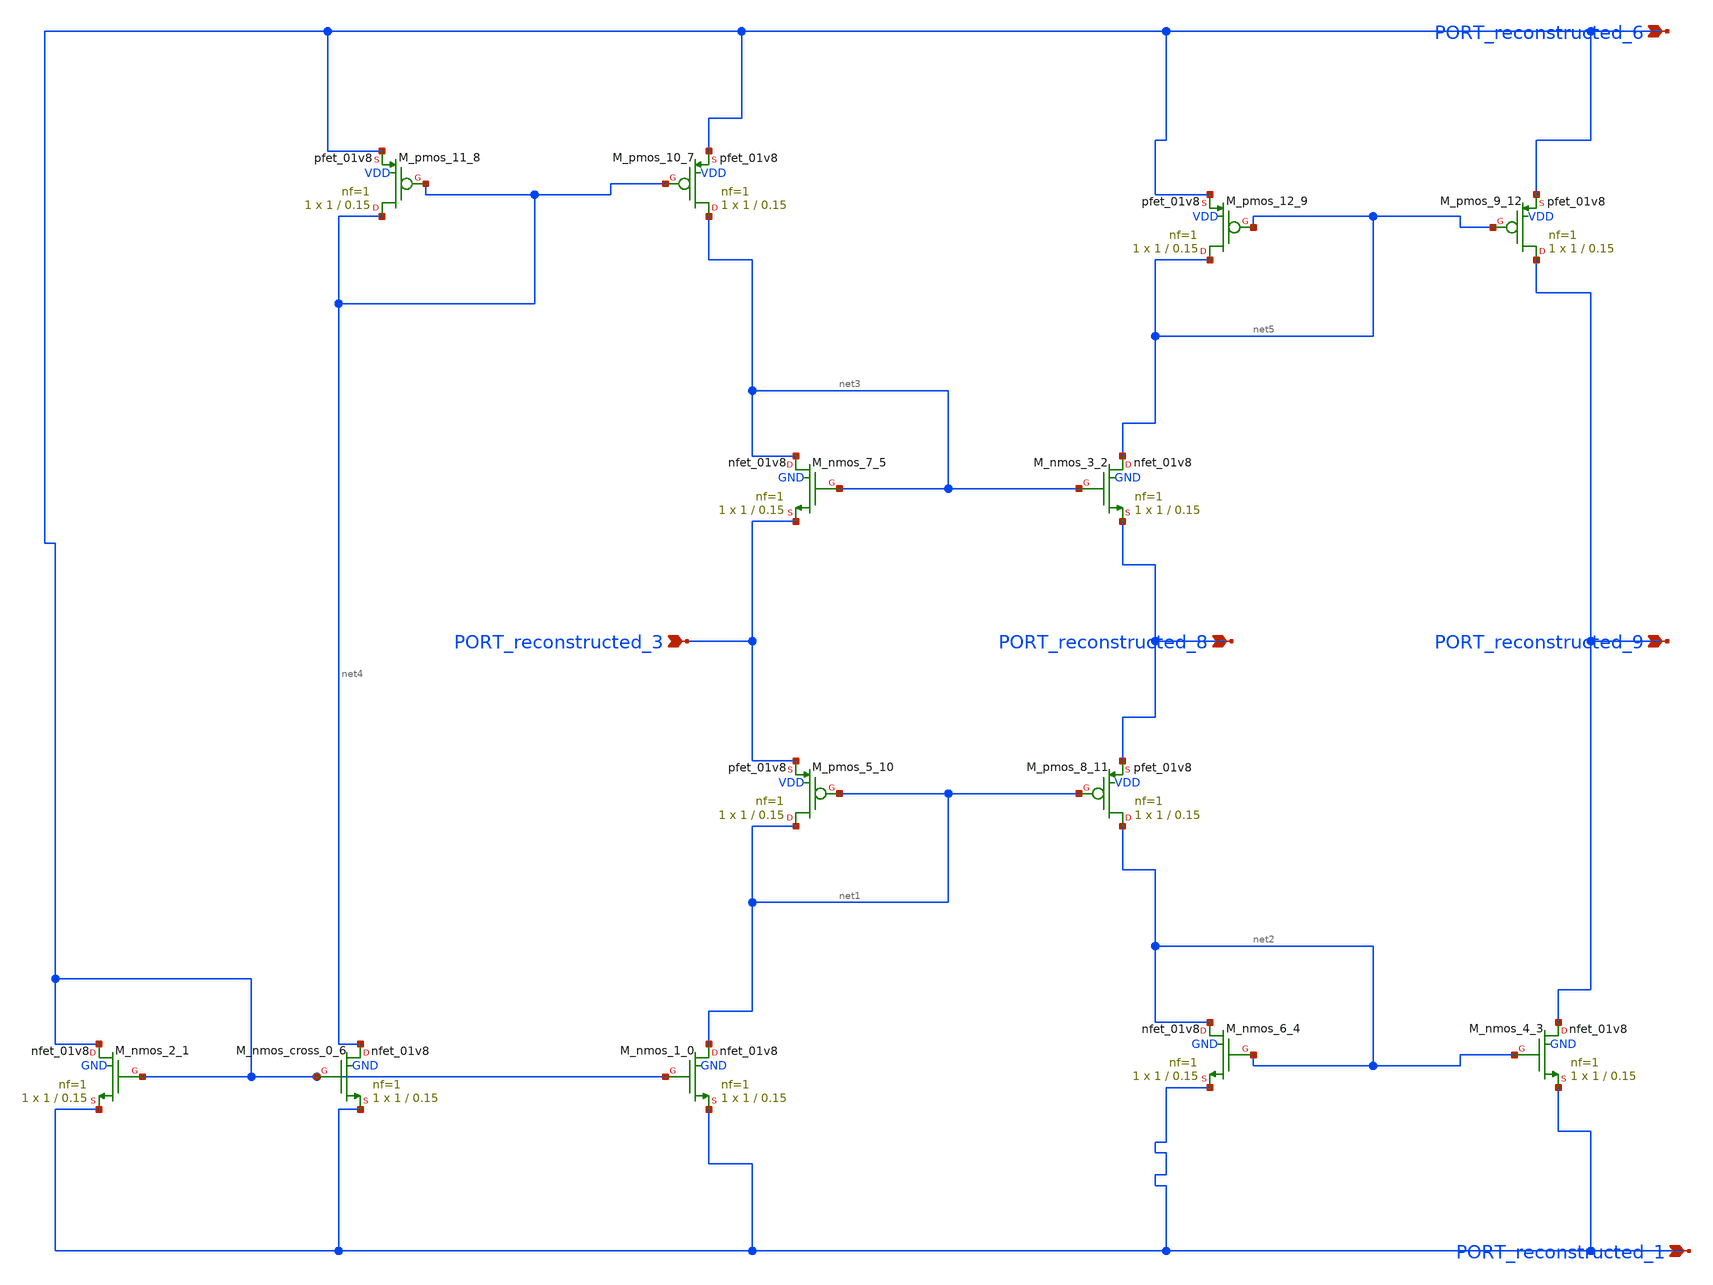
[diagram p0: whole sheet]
** sch_path: schematics/SchemGen/p06_fig1e_ccii.sch
**.subckt p06_fig1e_ccii PORT_reconstructed_8 PORT_reconstructed_3 PORT_reconstructed_9
*+ PORT_reconstructed_1 PORT_reconstructed_6
*.ipin PORT_reconstructed_8
*.ipin PORT_reconstructed_3
*.ipin PORT_reconstructed_9
*.ipin PORT_reconstructed_1
*.ipin PORT_reconstructed_6
XM_nmos_1_0 net1 PORT_reconstructed_6 PORT_reconstructed_1 GND sky130_fd_pr__nfet_01v8 L=0.15 W=1 nf=1
+ ad='int((1 + 1)/2) * 1 / 1 * 0.29' as='int((1 + 2)/2) * 1 / 1 * 0.29' pd='2*int((1 + 1)/2) * (1 / 1 + 0.29)'
+ ps='2*int((1 + 2)/2) * (1 / 1 + 0.29)' nrd='0.29 / 1 ' nrs='0.29 / 1 ' sa=0 sb=0 sd=0 mult=1 m=1
XM_nmos_2_1 PORT_reconstructed_6 PORT_reconstructed_6 PORT_reconstructed_1 GND sky130_fd_pr__nfet_01v8
+ L=0.15 W=1 nf=1 ad='int((1 + 1)/2) * 1 / 1 * 0.29' as='int((1 + 2)/2) * 1 / 1 * 0.29' pd='2*int((1 + 1)/2) * (1 / 1 + 0.29)'
+ ps='2*int((1 + 2)/2) * (1 / 1 + 0.29)' nrd='0.29 / 1 ' nrs='0.29 / 1 ' sa=0 sb=0 sd=0 mult=1 m=1
XM_nmos_3_2 net5 net3 PORT_reconstructed_8 GND sky130_fd_pr__nfet_01v8 L=0.15 W=1 nf=1 ad='int((1 + 1)/2) * 1 / 1 * 0.29'
+ as='int((1 + 2)/2) * 1 / 1 * 0.29' pd='2*int((1 + 1)/2) * (1 / 1 + 0.29)' ps='2*int((1 + 2)/2) * (1 / 1 + 0.29)'
+ nrd='0.29 / 1 ' nrs='0.29 / 1 ' sa=0 sb=0 sd=0 mult=1 m=1
XM_nmos_4_3 PORT_reconstructed_9 net2 PORT_reconstructed_1 GND sky130_fd_pr__nfet_01v8 L=0.15 W=1 nf=1
+ ad='int((1 + 1)/2) * 1 / 1 * 0.29' as='int((1 + 2)/2) * 1 / 1 * 0.29' pd='2*int((1 + 1)/2) * (1 / 1 + 0.29)'
+ ps='2*int((1 + 2)/2) * (1 / 1 + 0.29)' nrd='0.29 / 1 ' nrs='0.29 / 1 ' sa=0 sb=0 sd=0 mult=1 m=1
XM_nmos_6_4 net2 net2 PORT_reconstructed_1 GND sky130_fd_pr__nfet_01v8 L=0.15 W=1 nf=1 ad='int((1 + 1)/2) * 1 / 1 * 0.29'
+ as='int((1 + 2)/2) * 1 / 1 * 0.29' pd='2*int((1 + 1)/2) * (1 / 1 + 0.29)' ps='2*int((1 + 2)/2) * (1 / 1 + 0.29)'
+ nrd='0.29 / 1 ' nrs='0.29 / 1 ' sa=0 sb=0 sd=0 mult=1 m=1
XM_nmos_7_5 net3 net3 PORT_reconstructed_3 GND sky130_fd_pr__nfet_01v8 L=0.15 W=1 nf=1 ad='int((1 + 1)/2) * 1 / 1 * 0.29'
+ as='int((1 + 2)/2) * 1 / 1 * 0.29' pd='2*int((1 + 1)/2) * (1 / 1 + 0.29)' ps='2*int((1 + 2)/2) * (1 / 1 + 0.29)'
+ nrd='0.29 / 1 ' nrs='0.29 / 1 ' sa=0 sb=0 sd=0 mult=1 m=1
XM_nmos_cross_0_6 net4 PORT_reconstructed_6 PORT_reconstructed_1 GND sky130_fd_pr__nfet_01v8 L=0.15 W=1
+ nf=1 ad='int((1 + 1)/2) * 1 / 1 * 0.29' as='int((1 + 2)/2) * 1 / 1 * 0.29' pd='2*int((1 + 1)/2) * (1 / 1 + 0.29)'
+ ps='2*int((1 + 2)/2) * (1 / 1 + 0.29)' nrd='0.29 / 1 ' nrs='0.29 / 1 ' sa=0 sb=0 sd=0 mult=1 m=1
XM_pmos_10_7 net3 net4 PORT_reconstructed_6 VDD sky130_fd_pr__pfet_01v8 L=0.15 W=1 nf=1 ad='int((1 + 1)/2) * 1 / 1 * 0.29'
+ as='int((1 + 2)/2) * 1 / 1 * 0.29' pd='2*int((1 + 1)/2) * (1 / 1 + 0.29)' ps='2*int((1 + 2)/2) * (1 / 1 + 0.29)'
+ nrd='0.29 / 1 ' nrs='0.29 / 1 ' sa=0 sb=0 sd=0 mult=1 m=1
XM_pmos_11_8 net4 net4 PORT_reconstructed_6 VDD sky130_fd_pr__pfet_01v8 L=0.15 W=1 nf=1 ad='int((1 + 1)/2) * 1 / 1 * 0.29'
+ as='int((1 + 2)/2) * 1 / 1 * 0.29' pd='2*int((1 + 1)/2) * (1 / 1 + 0.29)' ps='2*int((1 + 2)/2) * (1 / 1 + 0.29)'
+ nrd='0.29 / 1 ' nrs='0.29 / 1 ' sa=0 sb=0 sd=0 mult=1 m=1
XM_pmos_12_9 net5 net5 PORT_reconstructed_6 VDD sky130_fd_pr__pfet_01v8 L=0.15 W=1 nf=1 ad='int((1 + 1)/2) * 1 / 1 * 0.29'
+ as='int((1 + 2)/2) * 1 / 1 * 0.29' pd='2*int((1 + 1)/2) * (1 / 1 + 0.29)' ps='2*int((1 + 2)/2) * (1 / 1 + 0.29)'
+ nrd='0.29 / 1 ' nrs='0.29 / 1 ' sa=0 sb=0 sd=0 mult=1 m=1
XM_pmos_5_10 net1 net1 PORT_reconstructed_3 VDD sky130_fd_pr__pfet_01v8 L=0.15 W=1 nf=1 ad='int((1 + 1)/2) * 1 / 1 * 0.29'
+ as='int((1 + 2)/2) * 1 / 1 * 0.29' pd='2*int((1 + 1)/2) * (1 / 1 + 0.29)' ps='2*int((1 + 2)/2) * (1 / 1 + 0.29)'
+ nrd='0.29 / 1 ' nrs='0.29 / 1 ' sa=0 sb=0 sd=0 mult=1 m=1
XM_pmos_8_11 net2 net1 PORT_reconstructed_8 VDD sky130_fd_pr__pfet_01v8 L=0.15 W=1 nf=1 ad='int((1 + 1)/2) * 1 / 1 * 0.29'
+ as='int((1 + 2)/2) * 1 / 1 * 0.29' pd='2*int((1 + 1)/2) * (1 / 1 + 0.29)' ps='2*int((1 + 2)/2) * (1 / 1 + 0.29)'
+ nrd='0.29 / 1 ' nrs='0.29 / 1 ' sa=0 sb=0 sd=0 mult=1 m=1
XM_pmos_9_12 PORT_reconstructed_9 net5 PORT_reconstructed_6 VDD sky130_fd_pr__pfet_01v8 L=0.15 W=1 nf=1
+ ad='int((1 + 1)/2) * 1 / 1 * 0.29' as='int((1 + 2)/2) * 1 / 1 * 0.29' pd='2*int((1 + 1)/2) * (1 / 1 + 0.29)'
+ ps='2*int((1 + 2)/2) * (1 / 1 + 0.29)' nrd='0.29 / 1 ' nrs='0.29 / 1 ' sa=0 sb=0 sd=0 mult=1 m=1
**.ends
.end
